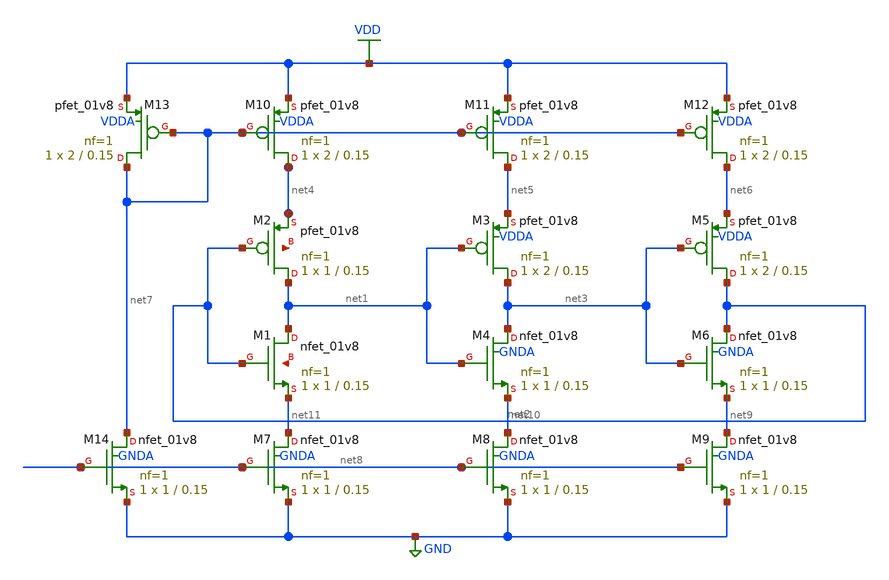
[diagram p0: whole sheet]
** sch_path: projects/pll/vco/xschem_ngspice/current_starved_VCO.sch
**.subckt current_starved_VCO
XM3 net3 net1 net5 VDDA sky130_fd_pr__pfet_01v8 L=0.15 W=2 nf=1 ad='int((nf+1)/2) * W/nf * 0.29' as='int((nf+2)/2) * W/nf * 0.29'
+ pd='2*int((nf+1)/2) * (W/nf + 0.29)' ps='2*int((nf+2)/2) * (W/nf + 0.29)' nrd='0.29 / W' nrs='0.29 / W'
+ sa=0 sb=0 sd=0 mult=1 m=1
XM4 net3 net1 net10 GNDA sky130_fd_pr__nfet_01v8 L=0.15 W=1 nf=1 ad='int((nf+1)/2) * W/nf * 0.29' as='int((nf+2)/2) * W/nf * 0.29'
+ pd='2*int((nf+1)/2) * (W/nf + 0.29)' ps='2*int((nf+2)/2) * (W/nf + 0.29)' nrd='0.29 / W' nrs='0.29 / W'
+ sa=0 sb=0 sd=0 mult=1 m=1
XM5 net2 net3 net6 VDDA sky130_fd_pr__pfet_01v8 L=0.15 W=2 nf=1 ad='int((nf+1)/2) * W/nf * 0.29' as='int((nf+2)/2) * W/nf * 0.29'
+ pd='2*int((nf+1)/2) * (W/nf + 0.29)' ps='2*int((nf+2)/2) * (W/nf + 0.29)' nrd='0.29 / W' nrs='0.29 / W'
+ sa=0 sb=0 sd=0 mult=1 m=1
XM6 net2 net3 net9 GNDA sky130_fd_pr__nfet_01v8 L=0.15 W=1 nf=1 ad='int((nf+1)/2) * W/nf * 0.29' as='int((nf+2)/2) * W/nf * 0.29'
+ pd='2*int((nf+1)/2) * (W/nf + 0.29)' ps='2*int((nf+2)/2) * (W/nf + 0.29)' nrd='0.29 / W' nrs='0.29 / W'
+ sa=0 sb=0 sd=0 mult=1 m=1
XM7 net11 net8 GND GNDA sky130_fd_pr__nfet_01v8 L=0.15 W=1 nf=1 ad='int((nf+1)/2) * W/nf * 0.29' as='int((nf+2)/2) * W/nf * 0.29'
+ pd='2*int((nf+1)/2) * (W/nf + 0.29)' ps='2*int((nf+2)/2) * (W/nf + 0.29)' nrd='0.29 / W' nrs='0.29 / W'
+ sa=0 sb=0 sd=0 mult=1 m=1
XM8 net10 net8 GND GNDA sky130_fd_pr__nfet_01v8 L=0.15 W=1 nf=1 ad='int((nf+1)/2) * W/nf * 0.29' as='int((nf+2)/2) * W/nf * 0.29'
+ pd='2*int((nf+1)/2) * (W/nf + 0.29)' ps='2*int((nf+2)/2) * (W/nf + 0.29)' nrd='0.29 / W' nrs='0.29 / W'
+ sa=0 sb=0 sd=0 mult=1 m=1
XM9 net9 net8 GND GNDA sky130_fd_pr__nfet_01v8 L=0.15 W=1 nf=1 ad='int((nf+1)/2) * W/nf * 0.29' as='int((nf+2)/2) * W/nf * 0.29'
+ pd='2*int((nf+1)/2) * (W/nf + 0.29)' ps='2*int((nf+2)/2) * (W/nf + 0.29)' nrd='0.29 / W' nrs='0.29 / W'
+ sa=0 sb=0 sd=0 mult=1 m=1
XM10 net4 net7 VDD VDDA sky130_fd_pr__pfet_01v8 L=0.15 W=2 nf=1 ad='int((nf+1)/2) * W/nf * 0.29' as='int((nf+2)/2) * W/nf * 0.29'
+ pd='2*int((nf+1)/2) * (W/nf + 0.29)' ps='2*int((nf+2)/2) * (W/nf + 0.29)' nrd='0.29 / W' nrs='0.29 / W'
+ sa=0 sb=0 sd=0 mult=1 m=1
XM11 net5 net7 VDD VDDA sky130_fd_pr__pfet_01v8 L=0.15 W=2 nf=1 ad='int((nf+1)/2) * W/nf * 0.29' as='int((nf+2)/2) * W/nf * 0.29'
+ pd='2*int((nf+1)/2) * (W/nf + 0.29)' ps='2*int((nf+2)/2) * (W/nf + 0.29)' nrd='0.29 / W' nrs='0.29 / W'
+ sa=0 sb=0 sd=0 mult=1 m=1
XM12 net6 net7 VDD VDDA sky130_fd_pr__pfet_01v8 L=0.15 W=2 nf=1 ad='int((nf+1)/2) * W/nf * 0.29' as='int((nf+2)/2) * W/nf * 0.29'
+ pd='2*int((nf+1)/2) * (W/nf + 0.29)' ps='2*int((nf+2)/2) * (W/nf + 0.29)' nrd='0.29 / W' nrs='0.29 / W'
+ sa=0 sb=0 sd=0 mult=1 m=1
XM13 net7 net7 VDD VDDA sky130_fd_pr__pfet_01v8 L=0.15 W=2 nf=1 ad='int((nf+1)/2) * W/nf * 0.29' as='int((nf+2)/2) * W/nf * 0.29'
+ pd='2*int((nf+1)/2) * (W/nf + 0.29)' ps='2*int((nf+2)/2) * (W/nf + 0.29)' nrd='0.29 / W' nrs='0.29 / W'
+ sa=0 sb=0 sd=0 mult=1 m=1
XM14 net7 net8 GND GNDA sky130_fd_pr__nfet_01v8 L=0.15 W=1 nf=1 ad='int((nf+1)/2) * W/nf * 0.29' as='int((nf+2)/2) * W/nf * 0.29'
+ pd='2*int((nf+1)/2) * (W/nf + 0.29)' ps='2*int((nf+2)/2) * (W/nf + 0.29)' nrd='0.29 / W' nrs='0.29 / W'
+ sa=0 sb=0 sd=0 mult=1 m=1
XM1 net1 net2 net11 net12 sky130_fd_pr__nfet_01v8 L=0.15 W=1 nf=1 ad='int((nf+1)/2) * W/nf * 0.29' as='int((nf+2)/2) * W/nf * 0.29'
+ pd='2*int((nf+1)/2) * (W/nf + 0.29)' ps='2*int((nf+2)/2) * (W/nf + 0.29)' nrd='0.29 / W' nrs='0.29 / W'
+ sa=0 sb=0 sd=0 mult=1 m=1
XM2 net1 net2 net4 net13 sky130_fd_pr__pfet_01v8 L=0.15 W=1 nf=1 ad='int((nf+1)/2) * W/nf * 0.29' as='int((nf+2)/2) * W/nf * 0.29'
+ pd='2*int((nf+1)/2) * (W/nf + 0.29)' ps='2*int((nf+2)/2) * (W/nf + 0.29)' nrd='0.29 / W' nrs='0.29 / W'
+ sa=0 sb=0 sd=0 mult=1 m=1
**.ends
.GLOBAL VDD
.GLOBAL GND
.end
